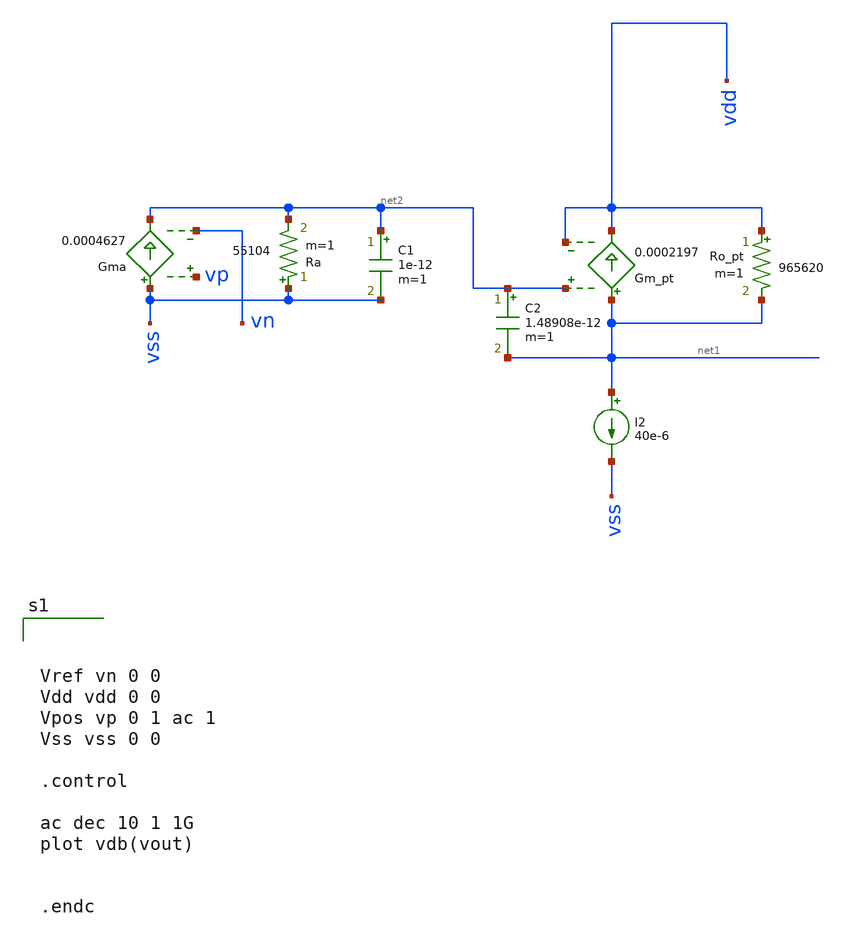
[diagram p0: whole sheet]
** sch_path: test/sstadex/xschem/stage2_OTA_tb.sch
**.subckt stage2_OTA_tb
Ro_pt vdd net1 965620 m=1
Gm_pt net1 vdd net2 vdd 0.0002197
Gma vss net2 vp vn 0.0004627
Ra vss net2 55104 m=1
I2 net1 vss 40e-6
C1 net2 vss 1e-12 m=1
C2 net2 net1 1.48908e-12 m=1
**** begin user architecture code



Vref vn 0 0
Vdd vdd 0 0
Vpos vp 0 1 ac 1
Vss vss 0 0

.control

ac dec 10 1 1G
plot vdb(vout)


.endc



**** end user architecture code
**.ends
.end
